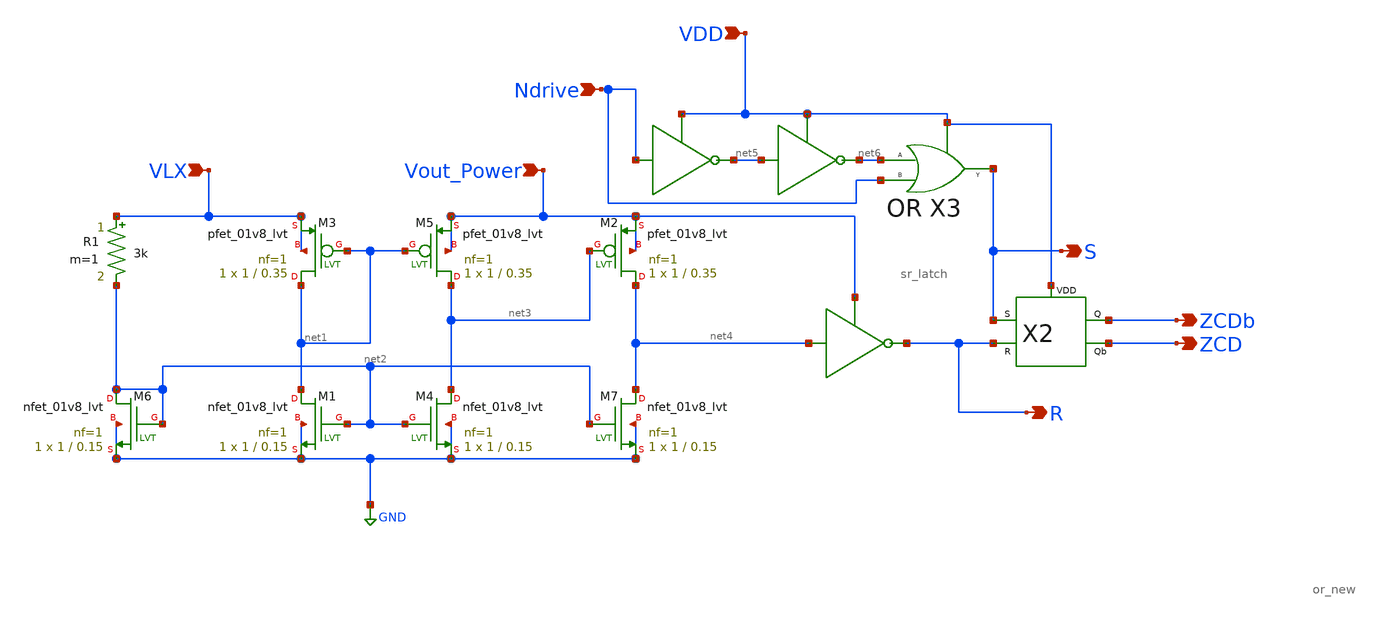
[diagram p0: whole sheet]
** sch_path: Current Sensor/zcd.sch
**.subckt zcd Vout_Power VLX Ndrive ZCD ZCDb VDD R S
*.ipin Vout_Power
*.ipin VLX
*.ipin Ndrive
*.opin ZCD
*.opin ZCDb
*.ipin VDD
*.opin R
*.opin S
XM1 net1 net2 GND GND sky130_fd_pr__nfet_01v8_lvt L=0.15 W=1 nf=1 ad='int((nf+1)/2) * W/nf * 0.29' as='int((nf+2)/2) * W/nf * 0.29'
+ pd='2*int((nf+1)/2) * (W/nf + 0.29)' ps='2*int((nf+2)/2) * (W/nf + 0.29)' nrd='0.29 / W' nrs='0.29 / W'
+ sa=0 sb=0 sd=0 mult=1 m=1
XM2 net4 net3 Vout_Power Vout_Power sky130_fd_pr__pfet_01v8_lvt L=0.35 W=1 nf=1 ad='int((nf+1)/2) * W/nf * 0.29'
+ as='int((nf+2)/2) * W/nf * 0.29' pd='2*int((nf+1)/2) * (W/nf + 0.29)' ps='2*int((nf+2)/2) * (W/nf + 0.29)'
+ nrd='0.29 / W' nrs='0.29 / W' sa=0 sb=0 sd=0 mult=1 m=1
XM3 net1 net1 VLX VLX sky130_fd_pr__pfet_01v8_lvt L=0.35 W=1 nf=1 ad='int((nf+1)/2) * W/nf * 0.29' as='int((nf+2)/2) * W/nf * 0.29'
+ pd='2*int((nf+1)/2) * (W/nf + 0.29)' ps='2*int((nf+2)/2) * (W/nf + 0.29)' nrd='0.29 / W' nrs='0.29 / W'
+ sa=0 sb=0 sd=0 mult=1 m=1
XM4 net3 net2 GND GND sky130_fd_pr__nfet_01v8_lvt L=0.15 W=1 nf=1 ad='int((nf+1)/2) * W/nf * 0.29' as='int((nf+2)/2) * W/nf * 0.29'
+ pd='2*int((nf+1)/2) * (W/nf + 0.29)' ps='2*int((nf+2)/2) * (W/nf + 0.29)' nrd='0.29 / W' nrs='0.29 / W'
+ sa=0 sb=0 sd=0 mult=1 m=1
XM5 net3 net1 Vout_Power Vout_Power sky130_fd_pr__pfet_01v8_lvt L=0.35 W=1 nf=1 ad='int((nf+1)/2) * W/nf * 0.29'
+ as='int((nf+2)/2) * W/nf * 0.29' pd='2*int((nf+1)/2) * (W/nf + 0.29)' ps='2*int((nf+2)/2) * (W/nf + 0.29)'
+ nrd='0.29 / W' nrs='0.29 / W' sa=0 sb=0 sd=0 mult=1 m=1
XM6 net2 net2 GND GND sky130_fd_pr__nfet_01v8_lvt L=0.15 W=1 nf=1 ad='int((nf+1)/2) * W/nf * 0.29' as='int((nf+2)/2) * W/nf * 0.29'
+ pd='2*int((nf+1)/2) * (W/nf + 0.29)' ps='2*int((nf+2)/2) * (W/nf + 0.29)' nrd='0.29 / W' nrs='0.29 / W'
+ sa=0 sb=0 sd=0 mult=1 m=1
XM7 net4 net2 GND GND sky130_fd_pr__nfet_01v8_lvt L=0.15 W=1 nf=1 ad='int((nf+1)/2) * W/nf * 0.29' as='int((nf+2)/2) * W/nf * 0.29'
+ pd='2*int((nf+1)/2) * (W/nf + 0.29)' ps='2*int((nf+2)/2) * (W/nf + 0.29)' nrd='0.29 / W' nrs='0.29 / W'
+ sa=0 sb=0 sd=0 mult=1 m=1
R1 VLX net2 3k m=1
X2 S R ZCDb ZCD VDD sr_latch
X3 Ndrive net6 S VDD or_new
**.ends

* expanding   symbol:  sr_latch.sym # of pins=5
** sym_path: Current Sensor/sr_latch.sym
** sch_path: Current Sensor/sr_latch.sch
.subckt sr_latch S R Q Qb VDD
*.ipin S
*.ipin R
*.opin Qb
*.opin Q
*.ipin VDD
XM9 net1 S GND GND sky130_fd_pr__nfet_01v8_lvt L=0.15 W=1 nf=1 ad='int((nf+1)/2) * W/nf * 0.29' as='int((nf+2)/2) * W/nf * 0.29'
+ pd='2*int((nf+1)/2) * (W/nf + 0.29)' ps='2*int((nf+2)/2) * (W/nf + 0.29)' nrd='0.29 / W' nrs='0.29 / W'
+ sa=0 sb=0 sd=0 mult=1 m=1
XM1 net2 R GND GND sky130_fd_pr__nfet_01v8_lvt L=0.15 W=1 nf=1 ad='int((nf+1)/2) * W/nf * 0.29' as='int((nf+2)/2) * W/nf * 0.29'
+ pd='2*int((nf+1)/2) * (W/nf + 0.29)' ps='2*int((nf+2)/2) * (W/nf + 0.29)' nrd='0.29 / W' nrs='0.29 / W'
+ sa=0 sb=0 sd=0 mult=1 m=1
XM2 Q Qb net1 net1 sky130_fd_pr__nfet_01v8_lvt L=0.15 W=1 nf=1 ad='int((nf+1)/2) * W/nf * 0.29' as='int((nf+2)/2) * W/nf * 0.29'
+ pd='2*int((nf+1)/2) * (W/nf + 0.29)' ps='2*int((nf+2)/2) * (W/nf + 0.29)' nrd='0.29 / W' nrs='0.29 / W'
+ sa=0 sb=0 sd=0 mult=1 m=1
XM3 Qb Q net2 net2 sky130_fd_pr__nfet_01v8_lvt L=0.15 W=1 nf=1 ad='int((nf+1)/2) * W/nf * 0.29' as='int((nf+2)/2) * W/nf * 0.29'
+ pd='2*int((nf+1)/2) * (W/nf + 0.29)' ps='2*int((nf+2)/2) * (W/nf + 0.29)' nrd='0.29 / W' nrs='0.29 / W'
+ sa=0 sb=0 sd=0 mult=1 m=1
XM5 Q S VDD VDD sky130_fd_pr__pfet_01v8_lvt L=0.45 W=1 nf=1 ad='int((nf+1)/2) * W/nf * 0.29' as='int((nf+2)/2) * W/nf * 0.29'
+ pd='2*int((nf+1)/2) * (W/nf + 0.29)' ps='2*int((nf+2)/2) * (W/nf + 0.29)' nrd='0.29 / W' nrs='0.29 / W'
+ sa=0 sb=0 sd=0 mult=1 m=1
XM6 Qb Q VDD VDD sky130_fd_pr__pfet_01v8_lvt L=0.45 W=1 nf=1 ad='int((nf+1)/2) * W/nf * 0.29' as='int((nf+2)/2) * W/nf * 0.29'
+ pd='2*int((nf+1)/2) * (W/nf + 0.29)' ps='2*int((nf+2)/2) * (W/nf + 0.29)' nrd='0.29 / W' nrs='0.29 / W'
+ sa=0 sb=0 sd=0 mult=1 m=1
XM7 Q Qb VDD VDD sky130_fd_pr__pfet_01v8_lvt L=0.45 W=1 nf=1 ad='int((nf+1)/2) * W/nf * 0.29' as='int((nf+2)/2) * W/nf * 0.29'
+ pd='2*int((nf+1)/2) * (W/nf + 0.29)' ps='2*int((nf+2)/2) * (W/nf + 0.29)' nrd='0.29 / W' nrs='0.29 / W'
+ sa=0 sb=0 sd=0 mult=1 m=1
XM8 Qb R VDD VDD sky130_fd_pr__pfet_01v8_lvt L=0.45 W=1 nf=1 ad='int((nf+1)/2) * W/nf * 0.29' as='int((nf+2)/2) * W/nf * 0.29'
+ pd='2*int((nf+1)/2) * (W/nf + 0.29)' ps='2*int((nf+2)/2) * (W/nf + 0.29)' nrd='0.29 / W' nrs='0.29 / W'
+ sa=0 sb=0 sd=0 mult=1 m=1
.ends


* expanding   symbol:  or_new.sym # of pins=4
** sym_path: Current Sensor/or_new.sym
** sch_path: Current Sensor/or_new.sch
.subckt or_new B A Y VDD
*.ipin VDD
*.ipin A
*.ipin B
*.opin Y
XM1 net1 A GND GND sky130_fd_pr__nfet_01v8_lvt L=0.15 W=1 nf=1 ad='int((nf+1)/2) * W/nf * 0.29' as='int((nf+2)/2) * W/nf * 0.29'
+ pd='2*int((nf+1)/2) * (W/nf + 0.29)' ps='2*int((nf+2)/2) * (W/nf + 0.29)' nrd='0.29 / W' nrs='0.29 / W'
+ sa=0 sb=0 sd=0 mult=1 m=1
XM2 net1 B net2 VDD sky130_fd_pr__pfet_01v8_lvt L=0.35 W=1 nf=1 ad='int((nf+1)/2) * W/nf * 0.29' as='int((nf+2)/2) * W/nf * 0.29'
+ pd='2*int((nf+1)/2) * (W/nf + 0.29)' ps='2*int((nf+2)/2) * (W/nf + 0.29)' nrd='0.29 / W' nrs='0.29 / W'
+ sa=0 sb=0 sd=0 mult=1 m=1
XM3 net2 A VDD VDD sky130_fd_pr__pfet_01v8_lvt L=0.35 W=1 nf=1 ad='int((nf+1)/2) * W/nf * 0.29' as='int((nf+2)/2) * W/nf * 0.29'
+ pd='2*int((nf+1)/2) * (W/nf + 0.29)' ps='2*int((nf+2)/2) * (W/nf + 0.29)' nrd='0.29 / W' nrs='0.29 / W'
+ sa=0 sb=0 sd=0 mult=1 m=1
XM4 net1 B GND GND sky130_fd_pr__nfet_01v8_lvt L=0.15 W=1 nf=1 ad='int((nf+1)/2) * W/nf * 0.29' as='int((nf+2)/2) * W/nf * 0.29'
+ pd='2*int((nf+1)/2) * (W/nf + 0.29)' ps='2*int((nf+2)/2) * (W/nf + 0.29)' nrd='0.29 / W' nrs='0.29 / W'
+ sa=0 sb=0 sd=0 mult=1 m=1
XM5 Y net1 VDD VDD sky130_fd_pr__pfet_01v8_lvt L=0.35 W=1 nf=1 ad='int((nf+1)/2) * W/nf * 0.29' as='int((nf+2)/2) * W/nf * 0.29'
+ pd='2*int((nf+1)/2) * (W/nf + 0.29)' ps='2*int((nf+2)/2) * (W/nf + 0.29)' nrd='0.29 / W' nrs='0.29 / W'
+ sa=0 sb=0 sd=0 mult=1 m=1
XM6 Y net1 GND GND sky130_fd_pr__nfet_01v8_lvt L=0.15 W=1 nf=1 ad='int((nf+1)/2) * W/nf * 0.29' as='int((nf+2)/2) * W/nf * 0.29'
+ pd='2*int((nf+1)/2) * (W/nf + 0.29)' ps='2*int((nf+2)/2) * (W/nf + 0.29)' nrd='0.29 / W' nrs='0.29 / W'
+ sa=0 sb=0 sd=0 mult=1 m=1
.ends

.GLOBAL GND
.end
